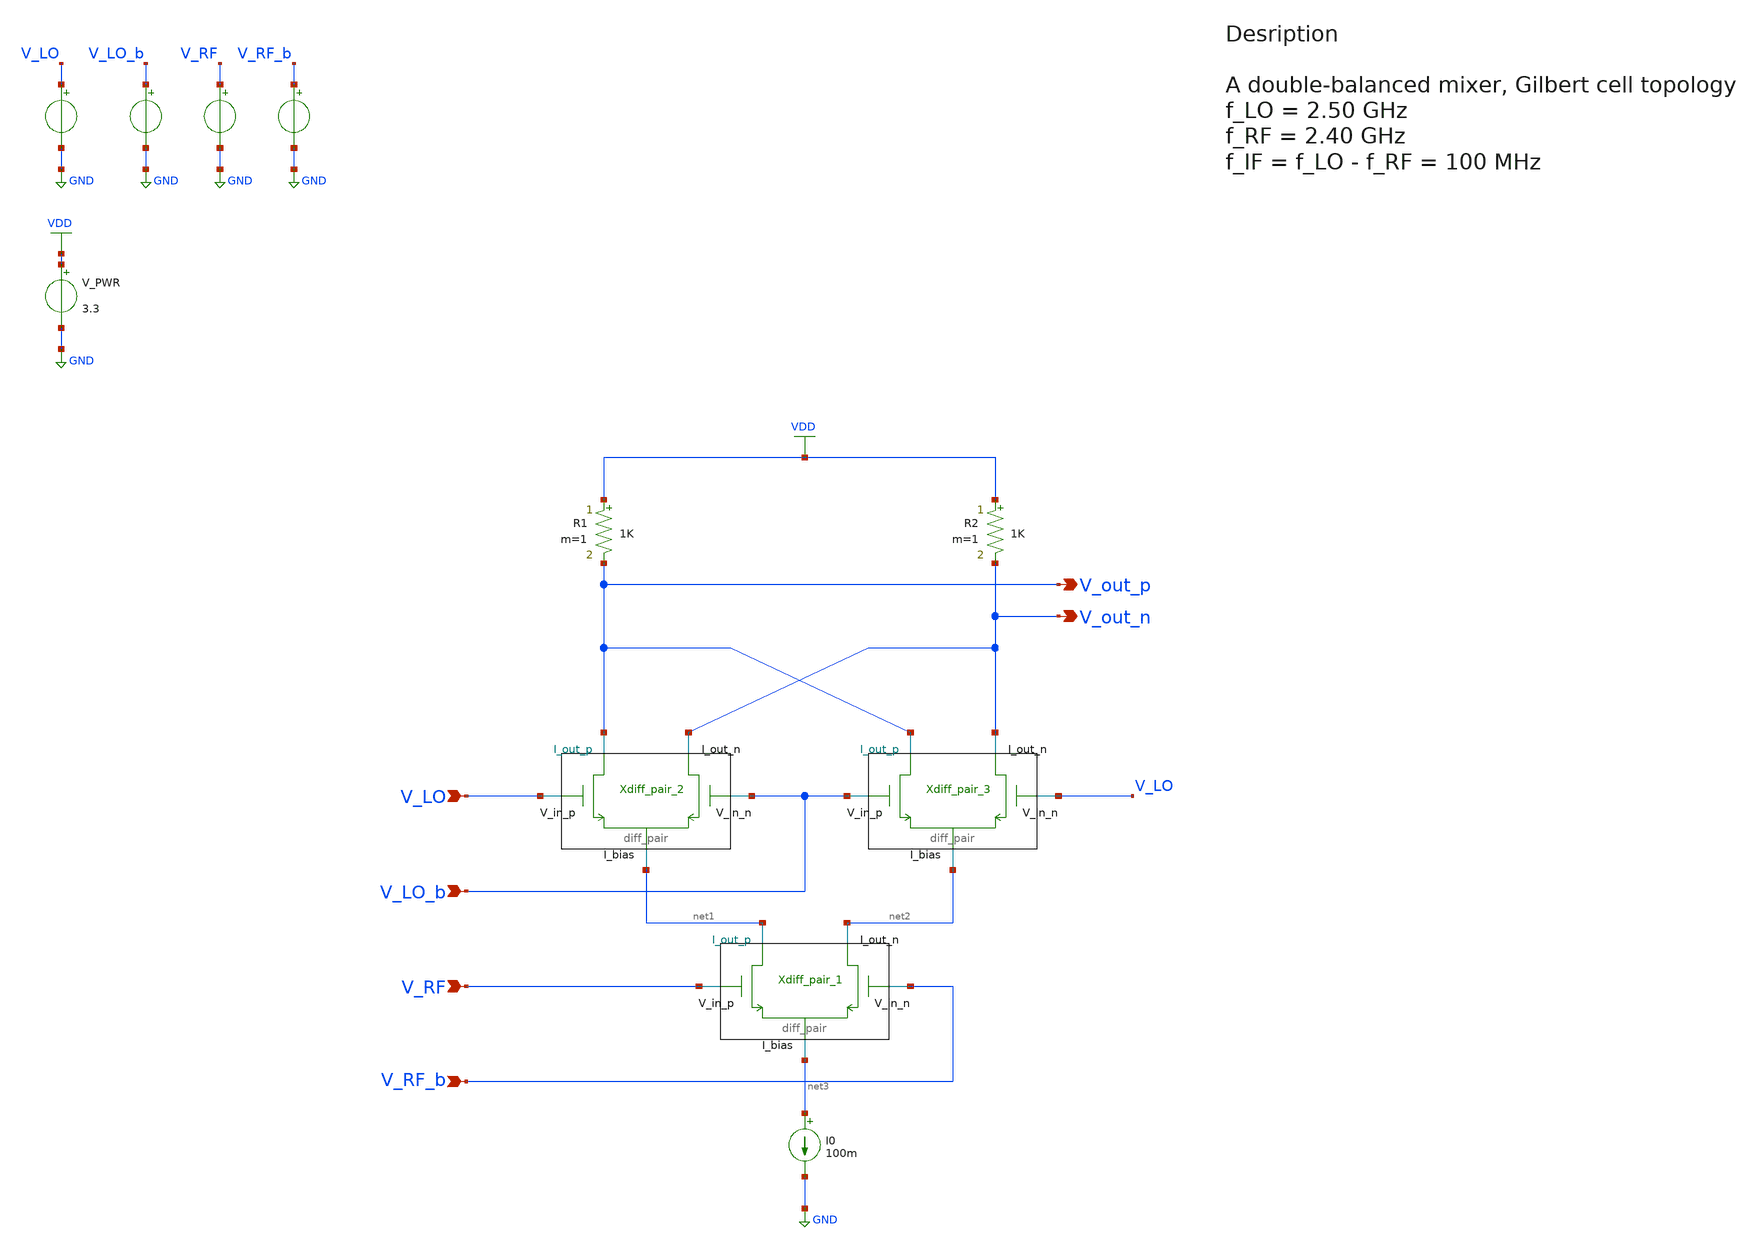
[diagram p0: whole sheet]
** sch_path: src/design_xsch/Gilbert_cell.sch
**.subckt Gilbert_cell V_LO V_LO_b V_RF V_RF_b V_out_p V_out_n
*.ipin V_LO
*.ipin V_LO_b
*.ipin V_RF
*.ipin V_RF_b
*.opin V_out_p
*.opin V_out_n
I0 net3 GND 100m
Xdiff_pair_1 net2 net1 V_RF V_RF_b net3 GND diff_pair W_neg=0.22u L_neg=0.28u W_pos=2u L_pos=0.28u
+ m=1
Xdiff_pair_2 V_out_n V_out_p V_LO V_LO_b net1 GND diff_pair W_neg=0.22u L_neg=0.28u W_pos=0.22u
+ L_pos=0.28u m=1
Xdiff_pair_3 V_out_n V_out_p V_LO_b V_LO net2 GND diff_pair W_neg=0.22u L_neg=0.28u W_pos=0.22u
+ L_pos=0.28u m=1
R1 VDD V_out_p 1K m=1
R2 VDD V_out_n 1K m=1
V_PWR VDD GND 3.3
.save i(v_pwr)
VLO V_LO GND sin(1.5 amp_lo freq_lo 0)
.save i(vlo)
VLOb V_LO_b GND sin(1.5 amp_lo freq_lo 0)
.save i(vlob)
V_RF V_RF GND sin(1.5 amp_rf freq_rf 0)
.save i(v_rf)
V_RFb V_RF_b GND sin(1.5 amp_rf freq_rf 0)
.save i(v_rfb)
**** begin user architecture code

.include $::180MCU_MODELS/design.ngspice
.lib $::180MCU_MODELS/sm141064.ngspice typical




* parameters used in the voltage source, initialization
.param freq_lo=2.5e9 amp_lo=2 dc_lo=1.5 freq_rf=1e9 amp_rf=2 dc_rf=1.5

.control

    * Set frequency and amplitude parameters to proper values from within the control sequence
    alterparam freq_lo = 2.50G
    alterparam amp_lo  = 0.25
    alterparam dc_lo   = 1.5
    alterparam freq_rf = 2.40G
    alterparam amp_rf  = 0.25
    reset

    save all

    * operating point
    op
    write Gilbert_sim.raw

    set appendwrite

    * Transient analysis to observe mixing operation
    tran 1p 10n
    write Gilbert_sim.raw
.endc


**** end user architecture code
**.ends

* expanding   symbol:  /home/vasil/Downloads/SSCS_PICO_2025/src/design_xsch/diff_pair.sym # of
*+ pins=5
** sym_path: src/design_xsch/diff_pair.sym
** sch_path: src/design_xsch/diff_pair.sch
.subckt diff_pair I_out_n I_out_p V_in_p V_in_n I_bias VSSPIN  mult=1  W_neg=0.22u L_neg=0.28u
+ W_pos=0.22u L_pos=0.28u
*.ipin V_in_p
*.ipin V_in_n
*.iopin I_out_p
*.iopin I_out_n
*.iopin I_bias
XM1 I_out_p V_in_p I_bias GND nfet_03v3 L=L_pos W=W_pos nf=1 ad='int((nf+1)/2) * W/nf * 0.18u' as='int((nf+2)/2) * W/nf * 0.18u'
+ pd='2*int((nf+1)/2) * (W/nf + 0.18u)' ps='2*int((nf+2)/2) * (W/nf + 0.18u)' nrd='0.18u / W' nrs='0.18u / W'
+ sa=0 sb=0 sd=0 m=mult
XM2 I_out_n V_in_n I_bias GND nfet_03v3 L=L_neg W=W_neg nf=1 ad='int((nf+1)/2) * W/nf * 0.18u' as='int((nf+2)/2) * W/nf * 0.18u'
+ pd='2*int((nf+1)/2) * (W/nf + 0.18u)' ps='2*int((nf+2)/2) * (W/nf + 0.18u)' nrd='0.18u / W' nrs='0.18u / W'
+ sa=0 sb=0 sd=0 m=mult
.ends

.GLOBAL VDD
.GLOBAL GND
.end
